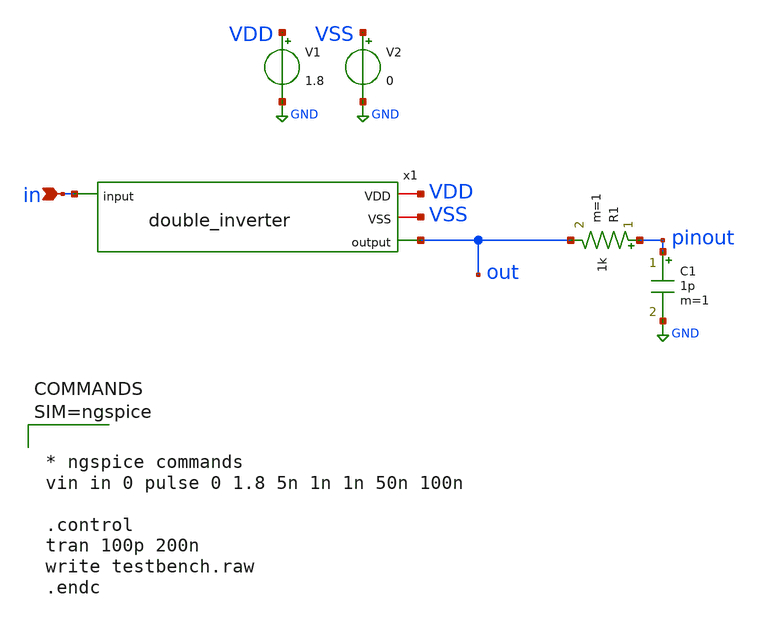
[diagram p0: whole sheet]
** sch_path: xschem/testbench.sch
**.subckt testbench in
*.ipin in
x1 VDD VSS out in double_inverter
V1 VDD GND 1.8
V2 VSS GND 0
R1 pinout out 1k m=1
C1 pinout GND 1p m=1
**** begin user architecture code

** opencircuitdesign pdks install
.lib $::SKYWATER_MODELS/sky130.lib.spice tt




* ngspice commands
vin in 0 pulse 0 1.8 5n 1n 1n 50n 100n

.control
tran 100p 200n
write testbench.raw
.endc





**** end user architecture code
**.ends

* expanding   symbol:  double_inverter.sym # of pins=4
** sym_path: xschem/double_inverter.sym
** sch_path: xschem/double_inverter.sch
.subckt double_inverter VDD VSS output input
*.iopin VDD
*.iopin VSS
*.ipin input
*.opin output
XM1 net1 input VDD VDD sky130_fd_pr__pfet_01v8 L=0.15 W=1 nf=1 ad='int((1 + 1)/2) * 1 / 1 * 0.29' as='int((1 + 2)/2) * 1 / 1 * 0.29'
+ pd='2*int((1 + 1)/2) * (1 / 1 + 0.29)' ps='2*int((1 + 2)/2) * (1 / 1 + 0.29)' nrd='0.29 / 1 ' nrs='0.29 / 1 '
+ sa=0 sb=0 sd=0 mult=1 m=1
XM2 net1 input VSS VSS sky130_fd_pr__nfet_01v8 L=0.15 W=1 nf=1 ad='int((1 + 1)/2) * 1 / 1 * 0.29' as='int((1 + 2)/2) * 1 / 1 * 0.29'
+ pd='2*int((1 + 1)/2) * (1 / 1 + 0.29)' ps='2*int((1 + 2)/2) * (1 / 1 + 0.29)' nrd='0.29 / 1 ' nrs='0.29 / 1 '
+ sa=0 sb=0 sd=0 mult=1 m=1
XM3 output net1 VDD VDD sky130_fd_pr__pfet_01v8 L=0.15 W=20 nf=20 ad='int((20 + 1)/2) * 20 / 20 * 0.29'
+ as='int((20 + 2)/2) * 20 / 20 * 0.29' pd='2*int((20 + 1)/2) * (20 / 20 + 0.29)' ps='2*int((20 + 2)/2) * (20 / 20 + 0.29)'
+ nrd='0.29 / 20 ' nrs='0.29 / 20 ' sa=0 sb=0 sd=0 mult=1 m=1
XM4 output net1 VSS VSS sky130_fd_pr__nfet_01v8 L=0.15 W=20 nf=20 ad='int((20 + 1)/2) * 20 / 20 * 0.29'
+ as='int((20 + 2)/2) * 20 / 20 * 0.29' pd='2*int((20 + 1)/2) * (20 / 20 + 0.29)' ps='2*int((20 + 2)/2) * (20 / 20 + 0.29)'
+ nrd='0.29 / 20 ' nrs='0.29 / 20 ' sa=0 sb=0 sd=0 mult=1 m=1
.ends

.GLOBAL GND
.end
